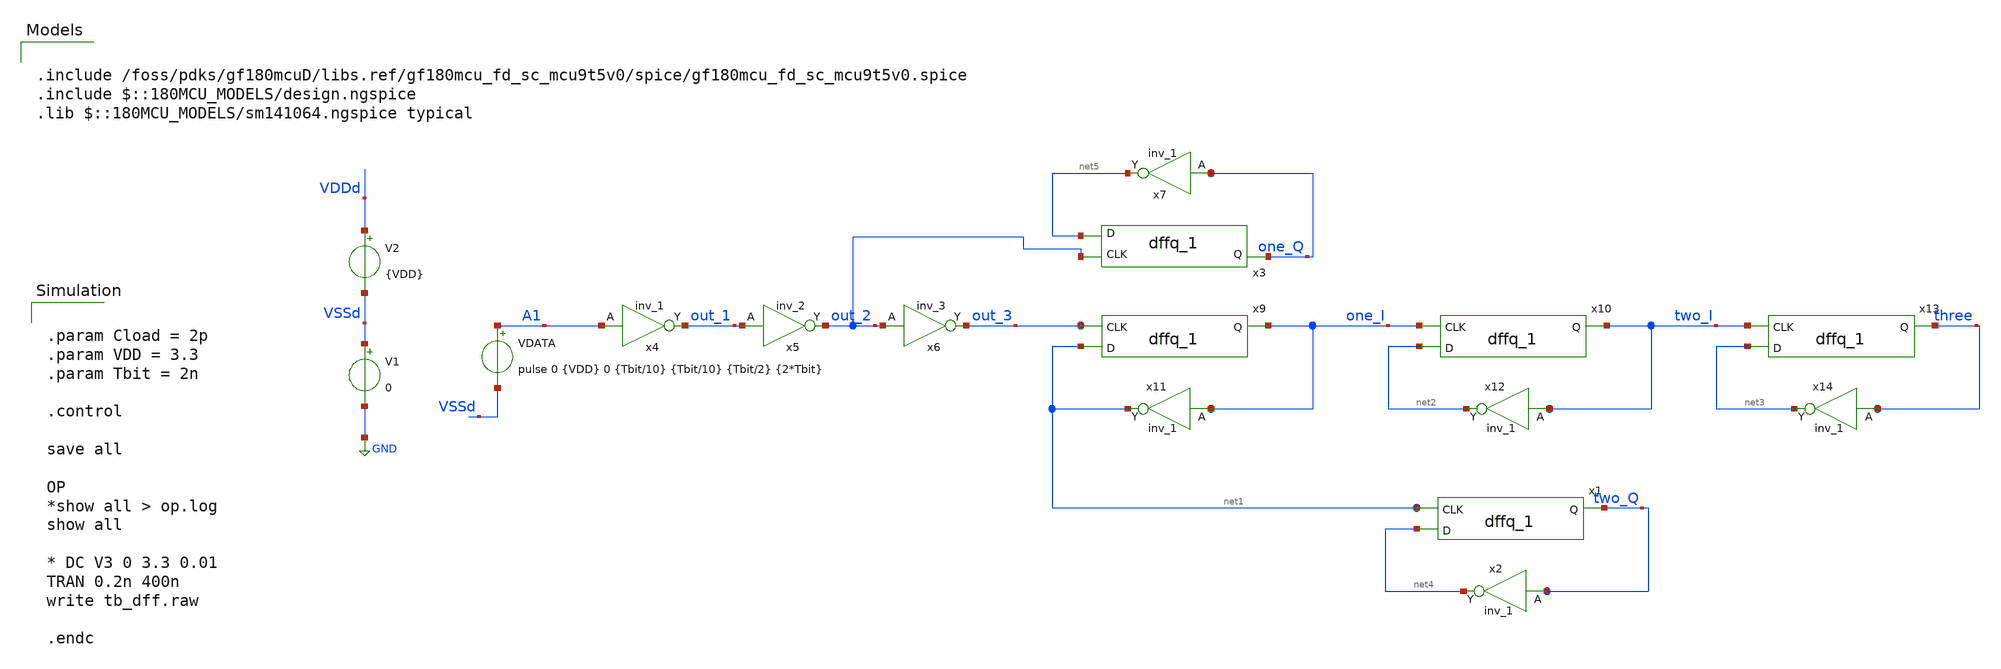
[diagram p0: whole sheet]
** sch_path: tb_digital_cells/tb_dff.sch
**.subckt tb_dff
V1 VSSd GND 0
V2 VDDd VSSd {VDD}
VDATA A1 VSSd pulse 0 {VDD} 0 {Tbit/10} {Tbit/10} {Tbit/2} {2*Tbit}
x4 A1 out_1 VDDd VDDd VSSd VSSd gf180mcu_fd_sc_mcu9t5v0__inv_1
x5 out_1 out_2 VDDd VDDd VSSd VSSd gf180mcu_fd_sc_mcu9t5v0__inv_2
x6 out_2 out_3 VDDd VDDd VSSd VSSd gf180mcu_fd_sc_mcu9t5v0__inv_3
x9 net1 out_3 one_I VDDd VDDd VSSd VSSd gf180mcu_fd_sc_mcu9t5v0__dffq_1
x11 one_I net1 VDDd VDDd VSSd VSSd gf180mcu_fd_sc_mcu9t5v0__inv_1
x10 net2 one_I two_I VDDd VDDd VSSd VSSd gf180mcu_fd_sc_mcu9t5v0__dffq_1
x12 two_I net2 VDDd VDDd VSSd VSSd gf180mcu_fd_sc_mcu9t5v0__inv_1
x13 net3 two_I three VDDd VDDd VSSd VSSd gf180mcu_fd_sc_mcu9t5v0__dffq_1
x14 three net3 VDDd VDDd VSSd VSSd gf180mcu_fd_sc_mcu9t5v0__inv_1
x1 net4 net1 two_Q VDDd VDDd VSSd VSSd gf180mcu_fd_sc_mcu9t5v0__dffq_1
x2 two_Q net4 VDDd VDDd VSSd VSSd gf180mcu_fd_sc_mcu9t5v0__inv_1
x3 net5 out_2 one_Q VDDd VDDd VSSd VSSd gf180mcu_fd_sc_mcu9t5v0__dffq_1
x7 one_Q net5 VDDd VDDd VSSd VSSd gf180mcu_fd_sc_mcu9t5v0__inv_1
**** begin user architecture code


.param Cload = 2p
.param VDD = 3.3
.param Tbit = 2n

.control

save all

OP
*show all > op.log
show all

* DC V3 0 3.3 0.01
TRAN 0.2n 400n
write tb_dff.raw

.endc



.include /foss/pdks/gf180mcuD/libs.ref/gf180mcu_fd_sc_mcu9t5v0/spice/gf180mcu_fd_sc_mcu9t5v0.spice
.include $::180MCU_MODELS/design.ngspice
.lib $::180MCU_MODELS/sm141064.ngspice typical

**** end user architecture code
**.ends
.GLOBAL GND
.end
